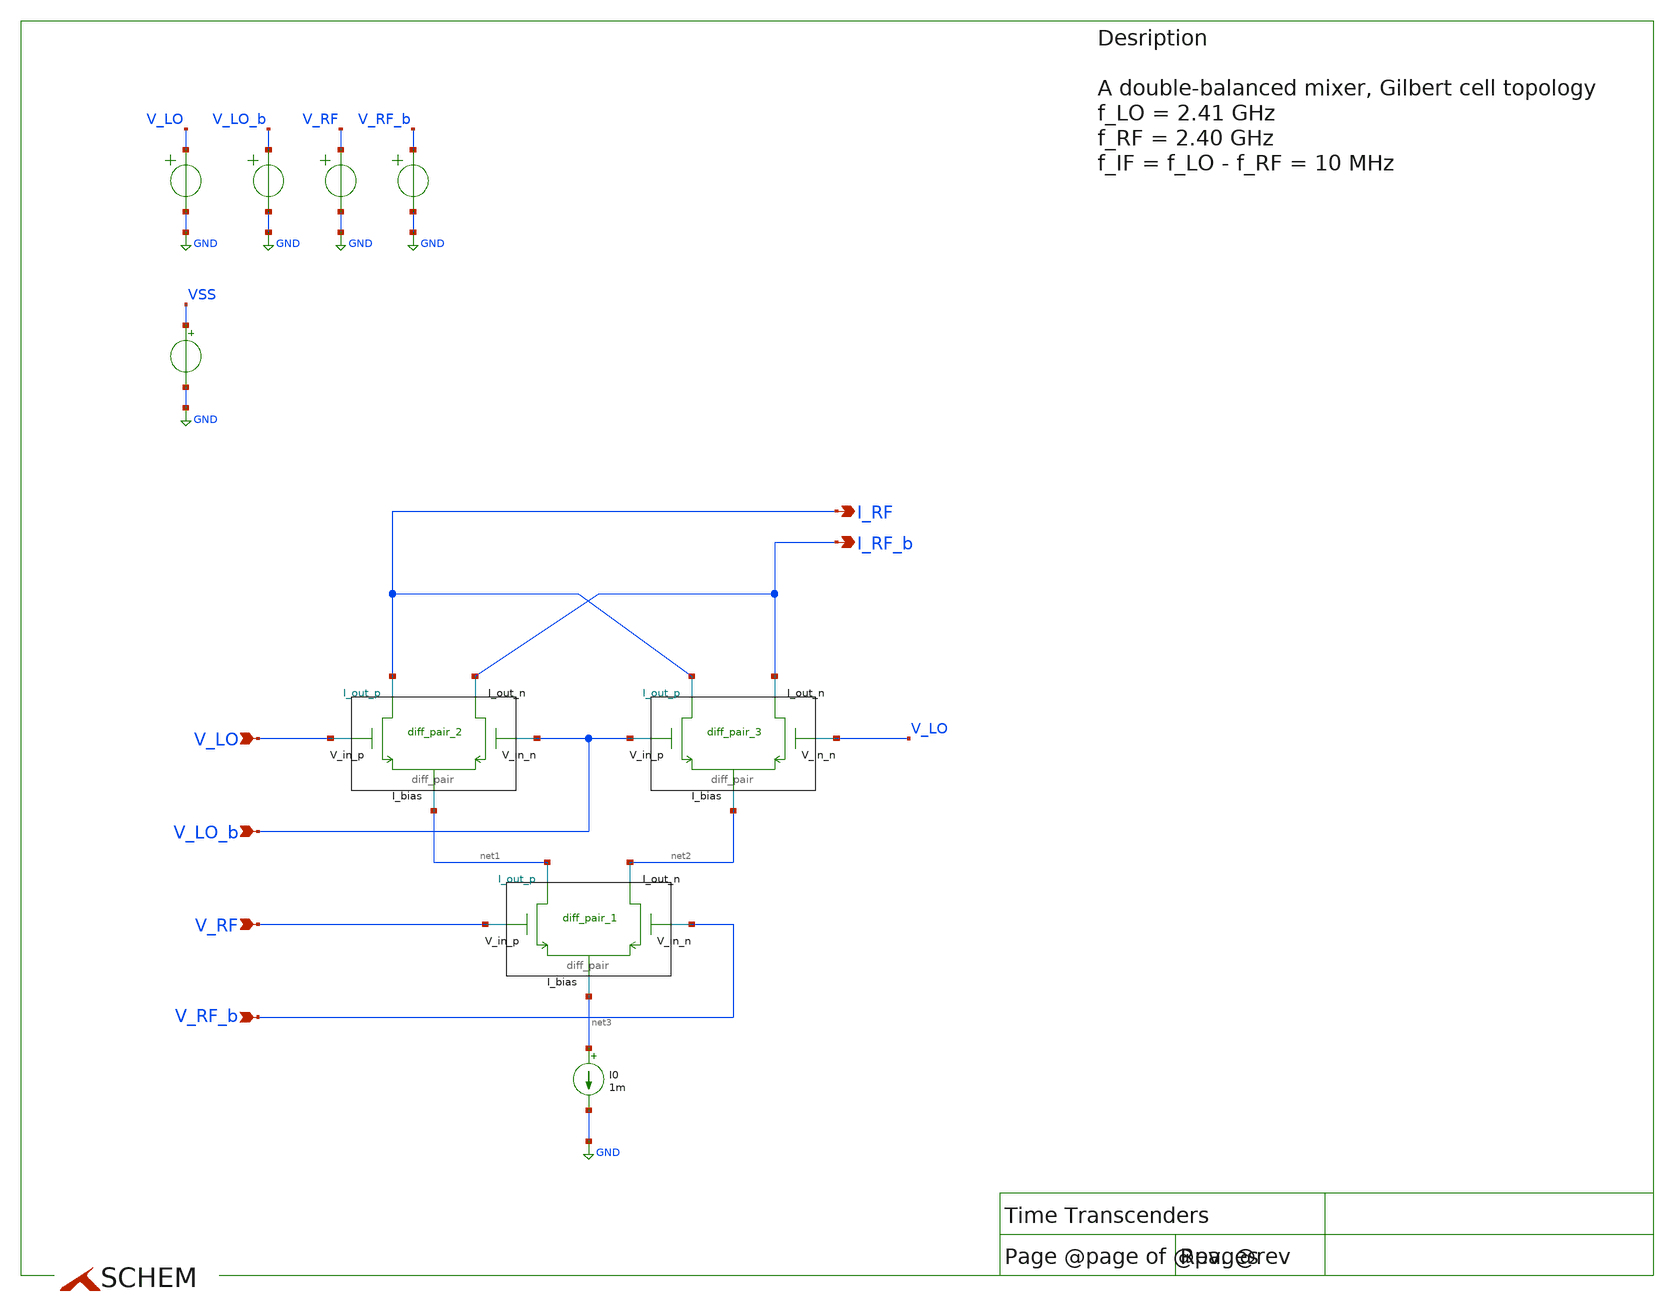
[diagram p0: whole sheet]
** sch_path: src/design_xsch/Gilbert_cell.sch
**.subckt Gilbert_cell V_LO V_LO_b V_RF V_RF_b I_RF I_RF_b
*.ipin V_LO
*.ipin V_LO_b
*.ipin V_RF
*.ipin V_RF_b
*.opin I_RF
*.opin I_RF_b
I0 net3 GND 1m
E1 V_LO GND VOL=' '1.5 + sin(time * 2.41 * 1e9)' '
E2 V_LO_b GND VOL=' '1.5 - sin(time * 2.41 * 1e9)' '
E4 V_RF GND VOL=' '1.5 + sin(time * 2.40 * 1e9)' '
E6 V_RF_b GND VOL=' '1.5 - sin(time * 2.40 * 1e9)' '
VSS VSS GND 0
diff_pair_1 net2 net1 V_RF V_RF_b net3 diff_pair VSS wn=1u ln=0.28u wp=1u lp=0.28u m=1
diff_pair_2 I_RF_b I_RF V_LO V_LO_b net1 diff_pair VSS wn=1u ln=0.28u wp=1u lp=0.28u m=1
diff_pair_3 I_RF_b I_RF V_LO_b V_LO net2 diff_pair VSS wn=1u ln=0.28u wp=1u lp=0.28u m=1
**** begin user architecture code

.include $::180MCU_MODELS/design.ngspice
.lib $::180MCU_MODELS/sm141064.ngspice typical



.temp 27
.control
save all
tran 1p 10n
write Gilbert_sim.raw
.endc


**** end user architecture code
**.ends

* expanding   symbol:  /home/vasil/Downloads/SSCS_PICO_2025/src/design_xsch/diff_pair.sym # of
*+ pins=5
** sym_path: src/design_xsch/diff_pair.sym
** sch_path: src/design_xsch/diff_pair.sch
.subckt diff_pair I_out_n I_out_p V_in_p V_in_n I_bias    wn=1u ln=0.28u wp=1u lp=0.28u
*.ipin V_in_p
*.ipin V_in_n
*.iopin I_out_p
*.iopin I_out_n
*.iopin I_bias
XM1 I_out_p V_in_p I_bias VSS nfet_03v3 L=lp W=wp nf=1 ad='int((nf+1)/2) * W/nf * 0.18u' as='int((nf+2)/2) * W/nf * 0.18u'
+ pd='2*int((nf+1)/2) * (W/nf + 0.18u)' ps='2*int((nf+2)/2) * (W/nf + 0.18u)' nrd='0.18u / W' nrs='0.18u / W'
+ sa=0 sb=0 sd=0 m=m
XM2 I_out_n V_in_n I_bias VSS nfet_03v3 L=ln W=wn nf=1 ad='int((nf+1)/2) * W/nf * 0.18u' as='int((nf+2)/2) * W/nf * 0.18u'
+ pd='2*int((nf+1)/2) * (W/nf + 0.18u)' ps='2*int((nf+2)/2) * (W/nf + 0.18u)' nrd='0.18u / W' nrs='0.18u / W'
+ sa=0 sb=0 sd=0 m=m
.ends

.GLOBAL GND
.GLOBAL VSS
.end
